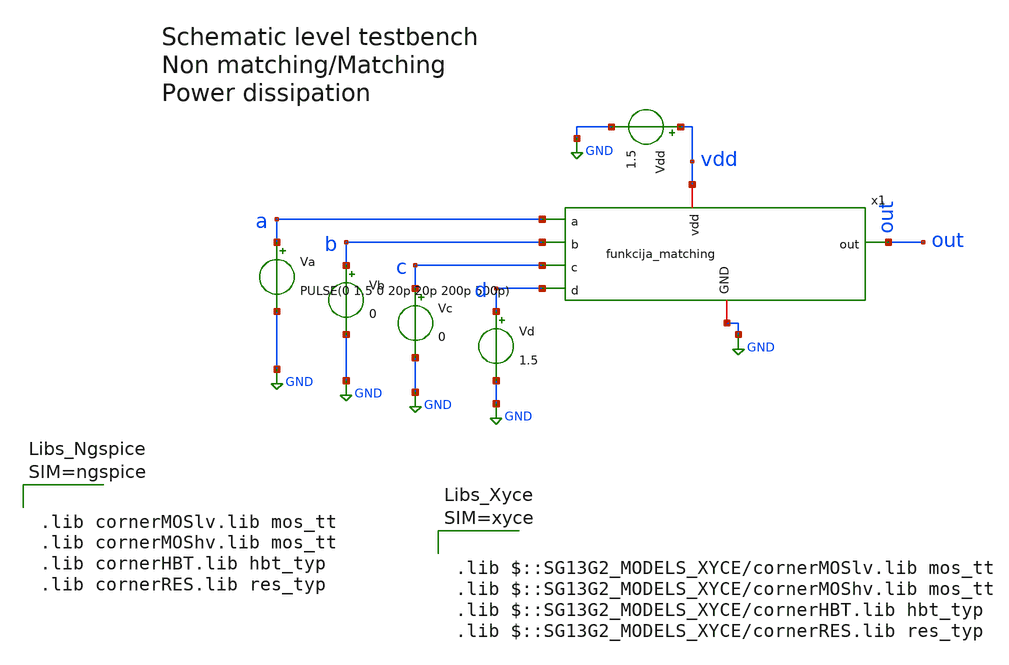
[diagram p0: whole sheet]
** sch_path: projekat/slucaj_2/pex/testbench/tb_powerdiss.sch
**.subckt tb_powerdiss
Va a GND PULSE(0 1.5 0 20p 20p 200p 500p)
Vb b GND 0
Vc c GND 0
Vd d GND 1.5
Vdd vdd GND 1.5
x1 vdd out d a c b GND funkcija_matching
**** begin user architecture code



.lib cornerMOSlv.lib mos_tt
.lib cornerMOShv.lib mos_tt
.lib cornerHBT.lib hbt_typ
.lib cornerRES.lib res_typ








.include /home/Nikola.Jankovic/projekat/slucaj_2/pex/funkcija_matching.spice
.tran 0.1p 500p
.control
  save all
  run

  * 1. STATIČKA SNAGA
  meas tran i_leak FIND i(Vdd) AT=450p
  let p_stat = abs(i_leak * 1.5)

  * 2. DINAMIČKA SNAGA
  meas tran i_total_avg AVG i(Vdd) from=0 to=500p
  let p_dyn = abs((i_total_avg - i_leak) * 1.5)

  print p_stat
  print p_dyn
.endc

**** end user architecture code
**.ends
.GLOBAL GND
.end
